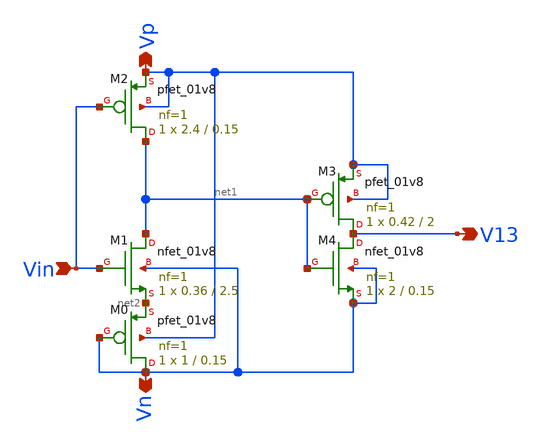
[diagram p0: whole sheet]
** sch_path: xschem/Vth_sch/Symbol/th13.sch
**.subckt th13 Vn Vp Vin V13
*.opin Vn
*.opin Vp
*.ipin Vin
*.opin V13
XM3 V13 net1 Vp Vp sky130_fd_pr__pfet_01v8 L=2 W=0.42 nf=1 ad='int((nf+1)/2) * W/nf * 0.29' as='int((nf+2)/2) * W/nf * 0.29'
+ pd='2*int((nf+1)/2) * (W/nf + 0.29)' ps='2*int((nf+2)/2) * (W/nf + 0.29)' nrd='0.29 / W' nrs='0.29 / W'
+ sa=0 sb=0 sd=0 mult=1 m=1
XM4 V13 net1 Vn Vn sky130_fd_pr__nfet_01v8 L=0.15 W=2 nf=1 ad='int((nf+1)/2) * W/nf * 0.29' as='int((nf+2)/2) * W/nf * 0.29'
+ pd='2*int((nf+1)/2) * (W/nf + 0.29)' ps='2*int((nf+2)/2) * (W/nf + 0.29)' nrd='0.29 / W' nrs='0.29 / W'
+ sa=0 sb=0 sd=0 mult=1 m=1
XM2 net1 Vin Vp Vp sky130_fd_pr__pfet_01v8 L=0.15 W=2.4 nf=1 ad='int((nf+1)/2) * W/nf * 0.29' as='int((nf+2)/2) * W/nf * 0.29'
+ pd='2*int((nf+1)/2) * (W/nf + 0.29)' ps='2*int((nf+2)/2) * (W/nf + 0.29)' nrd='0.29 / W' nrs='0.29 / W'
+ sa=0 sb=0 sd=0 mult=1 m=1
XM1 net1 Vin net2 Vn sky130_fd_pr__nfet_01v8 L=2.5 W=0.36 nf=1 ad='int((nf+1)/2) * W/nf * 0.29' as='int((nf+2)/2) * W/nf * 0.29'
+ pd='2*int((nf+1)/2) * (W/nf + 0.29)' ps='2*int((nf+2)/2) * (W/nf + 0.29)' nrd='0.29 / W' nrs='0.29 / W'
+ sa=0 sb=0 sd=0 mult=1 m=1
XM0 Vn Vn net2 Vp sky130_fd_pr__pfet_01v8 L=0.15 W=1 nf=1 ad='int((nf+1)/2) * W/nf * 0.29' as='int((nf+2)/2) * W/nf * 0.29'
+ pd='2*int((nf+1)/2) * (W/nf + 0.29)' ps='2*int((nf+2)/2) * (W/nf + 0.29)' nrd='0.29 / W' nrs='0.29 / W'
+ sa=0 sb=0 sd=0 mult=1 m=1
**.ends
.end
